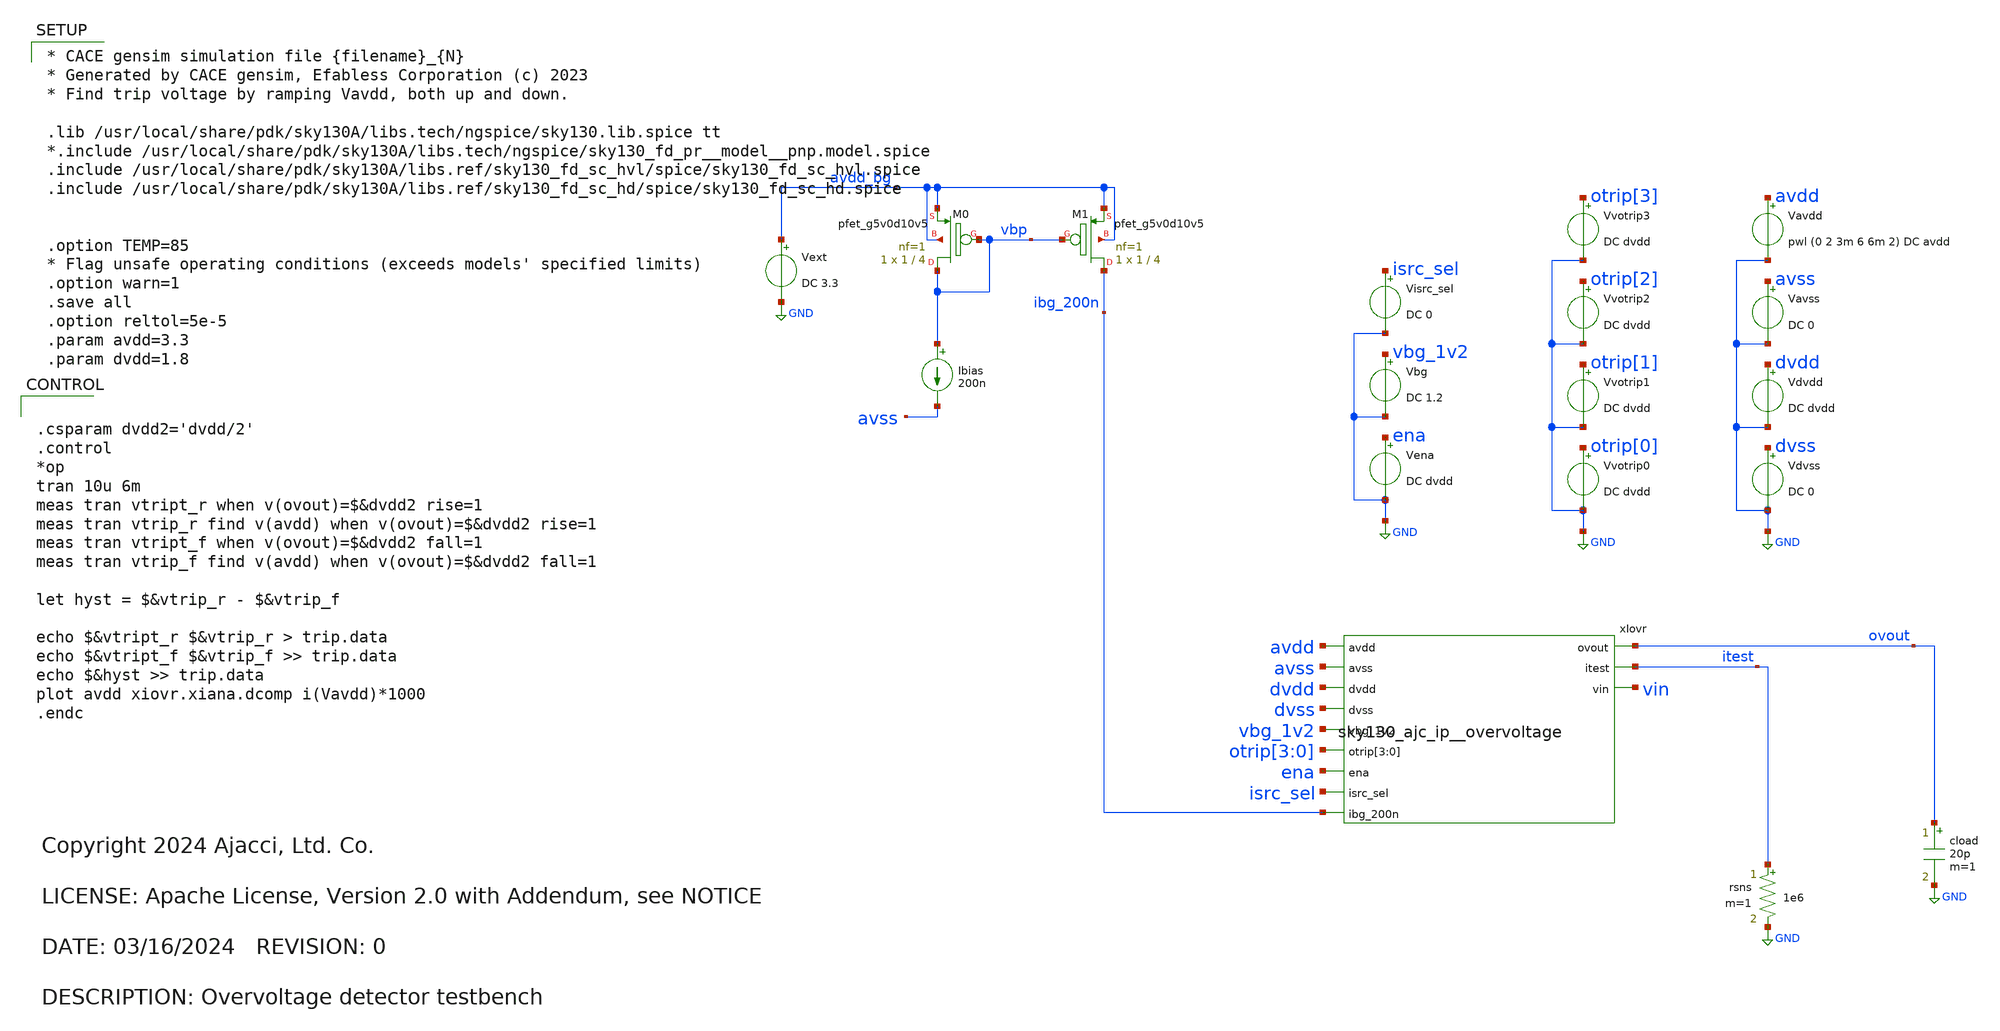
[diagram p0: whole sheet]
** sch_path: xschem/response_time.sch
* Copyright 2024 Ajacci, Ltd. Co.
* LICENSE: Apache License, Version 2.0 with Addendum, see NOTICE
**.subckt response_time
Vavss avss GND DC 0
Vena ena GND DC dvdd
Vavdd avdd GND pwl (0 2 3m 6 6m 2) DC avdd
.save i(vavdd)
Vbg vbg_1v2 GND DC 1.2
Ibias vbp avss 200n
XM1 ibg_200n vbp avdd_bg avdd_bg sky130_fd_pr__pfet_g5v0d10v5 L=4 W=1 nf=1 ad='int((nf+1)/2) * W/nf * 0.29'
+ as='int((nf+2)/2) * W/nf * 0.29' pd='2*int((nf+1)/2) * (W/nf + 0.29)' ps='2*int((nf+2)/2) * (W/nf + 0.29)'
+ nrd='0.29 / W' nrs='0.29 / W' sa=0 sb=0 sd=0 mult=1 m=1
XM0 vbp vbp avdd_bg avdd_bg sky130_fd_pr__pfet_g5v0d10v5 L=4 W=1 nf=1 ad='int((nf+1)/2) * W/nf * 0.29'
+ as='int((nf+2)/2) * W/nf * 0.29' pd='2*int((nf+1)/2) * (W/nf + 0.29)' ps='2*int((nf+2)/2) * (W/nf + 0.29)'
+ nrd='0.29 / W' nrs='0.29 / W' sa=0 sb=0 sd=0 mult=1 m=1
Vdvss dvss GND DC 0
Vdvdd dvdd GND DC dvdd
.save i(vdvdd)
rsns itest GND 1e6 m=1
cload ovout GND 20p m=1
xIovr avdd avss dvdd dvss vbg_1v2 ovout itest otrip[3] otrip[2] otrip[1] otrip[0] vin ena isrc_sel
+ ibg_200n sky130_ajc_ip__overvoltage
Vvotrip0 otrip[0] GND DC dvdd
.save i(vvotrip0)
Vvotrip1 otrip[1] GND DC dvdd
.save i(vvotrip1)
Vvotrip2 otrip[2] GND DC dvdd
.save i(vvotrip2)
Vvotrip3 otrip[3] GND DC dvdd
.save i(vvotrip3)
Visrc_sel isrc_sel GND DC 0
Vext avdd_bg GND DC 3.3
.save i(vext)
**** begin user architecture code

* CACE gensim simulation file {filename}_{N}
* Generated by CACE gensim, Efabless Corporation (c) 2023
* Find trip voltage by ramping Vavdd, both up and down.

.lib /usr/local/share/pdk/sky130A/libs.tech/ngspice/sky130.lib.spice tt
*.include /usr/local/share/pdk/sky130A/libs.tech/ngspice/sky130_fd_pr__model__pnp.model.spice
.include /usr/local/share/pdk/sky130A/libs.ref/sky130_fd_sc_hvl/spice/sky130_fd_sc_hvl.spice
.include /usr/local/share/pdk/sky130A/libs.ref/sky130_fd_sc_hd/spice/sky130_fd_sc_hd.spice


.option TEMP=85
* Flag unsafe operating conditions (exceeds models' specified limits)
.option warn=1
.save all
.option reltol=5e-5
.param avdd=3.3
.param dvdd=1.8





.csparam dvdd2='dvdd/2'
.control
*op
tran 10u 6m
meas tran vtript_r when v(ovout)=$&dvdd2 rise=1
meas tran vtrip_r find v(avdd) when v(ovout)=$&dvdd2 rise=1
meas tran vtript_f when v(ovout)=$&dvdd2 fall=1
meas tran vtrip_f find v(avdd) when v(ovout)=$&dvdd2 fall=1

let hyst = $&vtrip_r - $&vtrip_f

echo $&vtript_r $&vtrip_r > trip.data
echo $&vtript_f $&vtrip_f >> trip.data
echo $&hyst >> trip.data
plot avdd xiovr.xiana.dcomp i(Vavdd)*1000
.endc


**** end user architecture code
**.ends
.GLOBAL GND
.end
